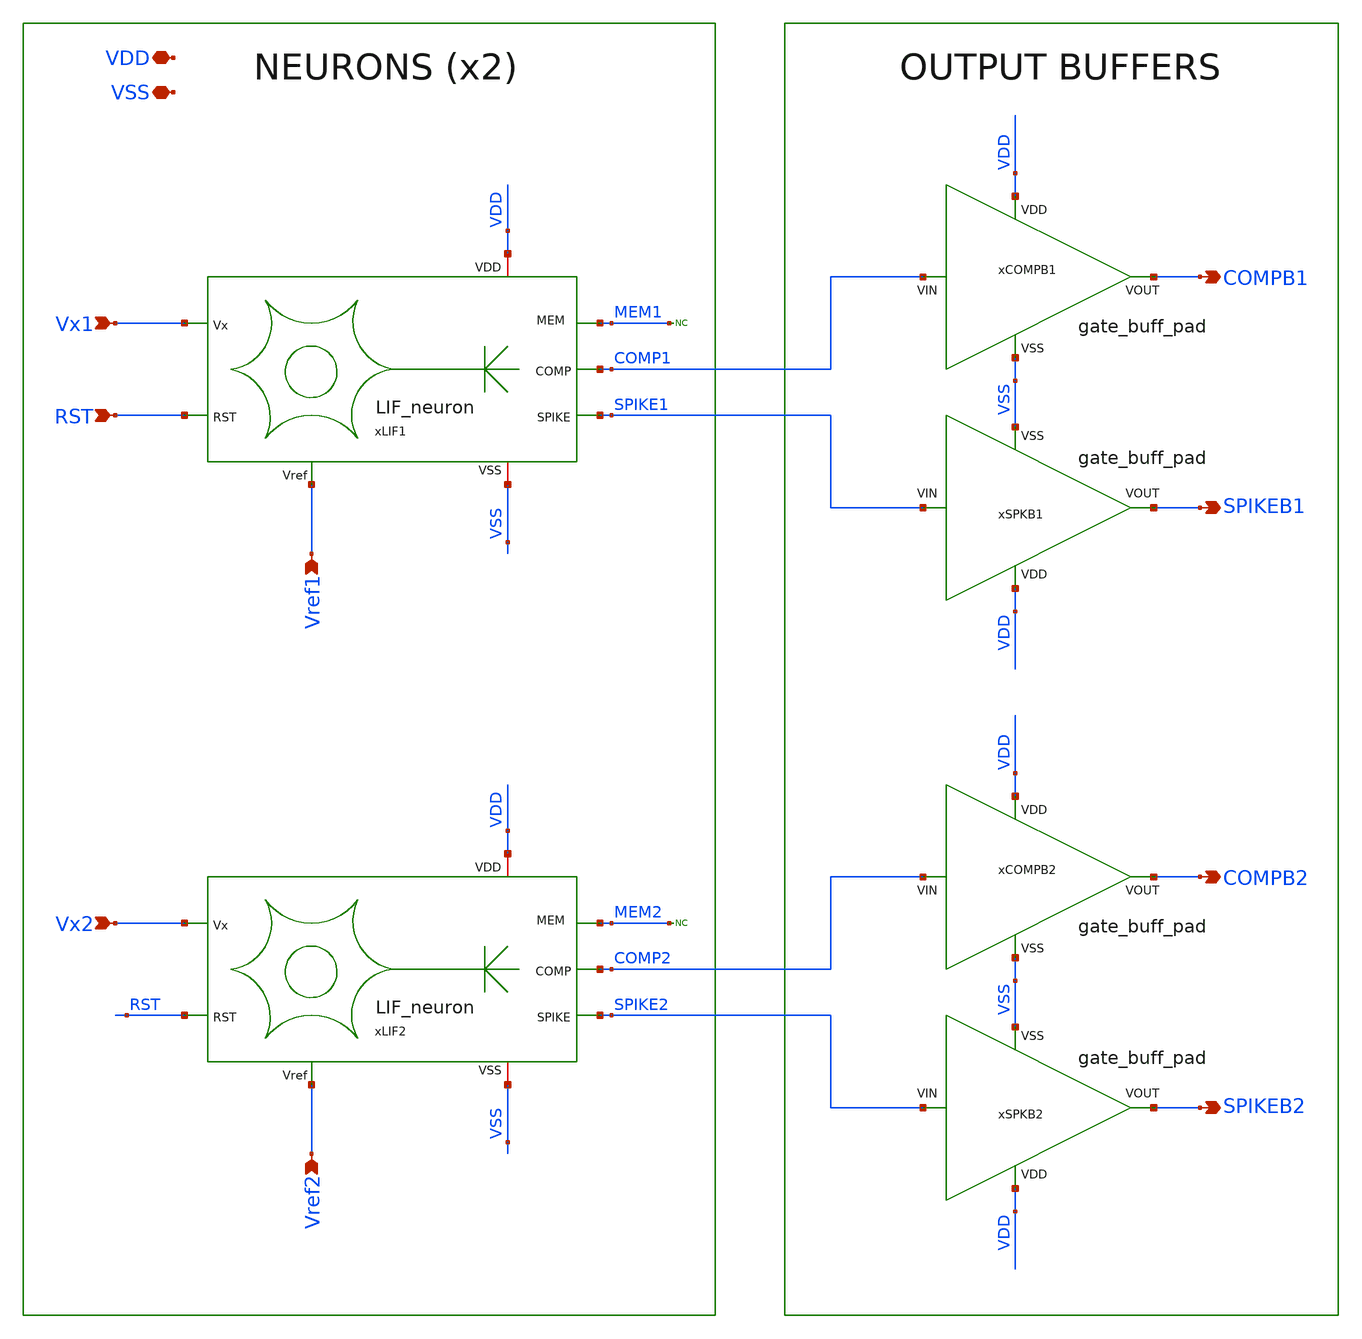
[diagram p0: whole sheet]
** sch_path: OSC9996-main/schematic/xschem/TOP_ROILIFNEURON.sch
**.subckt TOP_ROILIFNEURON SPIKEB1 COMPB1 SPIKEB2 COMPB2 VDD VSS Vx1 Vref1 Vx2 Vref2 RST
*.opin SPIKEB1
*.opin COMPB1
*.opin SPIKEB2
*.opin COMPB2
*.iopin VDD
*.iopin VSS
*.ipin Vx1
*.ipin Vref1
*.ipin Vx2
*.ipin Vref2
*.ipin RST
xSPKB1 VDD SPIKE1 SPIKEB1 VSS gate_buff_pad
xCOMPB1 VDD COMP1 COMPB1 VSS gate_buff_pad
* noconn MEM1
* noconn MEM2
xSPKB2 VDD SPIKE2 SPIKEB2 VSS gate_buff_pad
xCOMPB2 VDD COMP2 COMPB2 VSS gate_buff_pad
xLIF1 VDD Vx1 MEM1 RST SPIKE1 VSS Vref1 COMP1 LIF_neuron
xLIF2 VDD Vx2 MEM2 RST SPIKE2 VSS Vref2 COMP2 LIF_neuron
**.ends
.end
